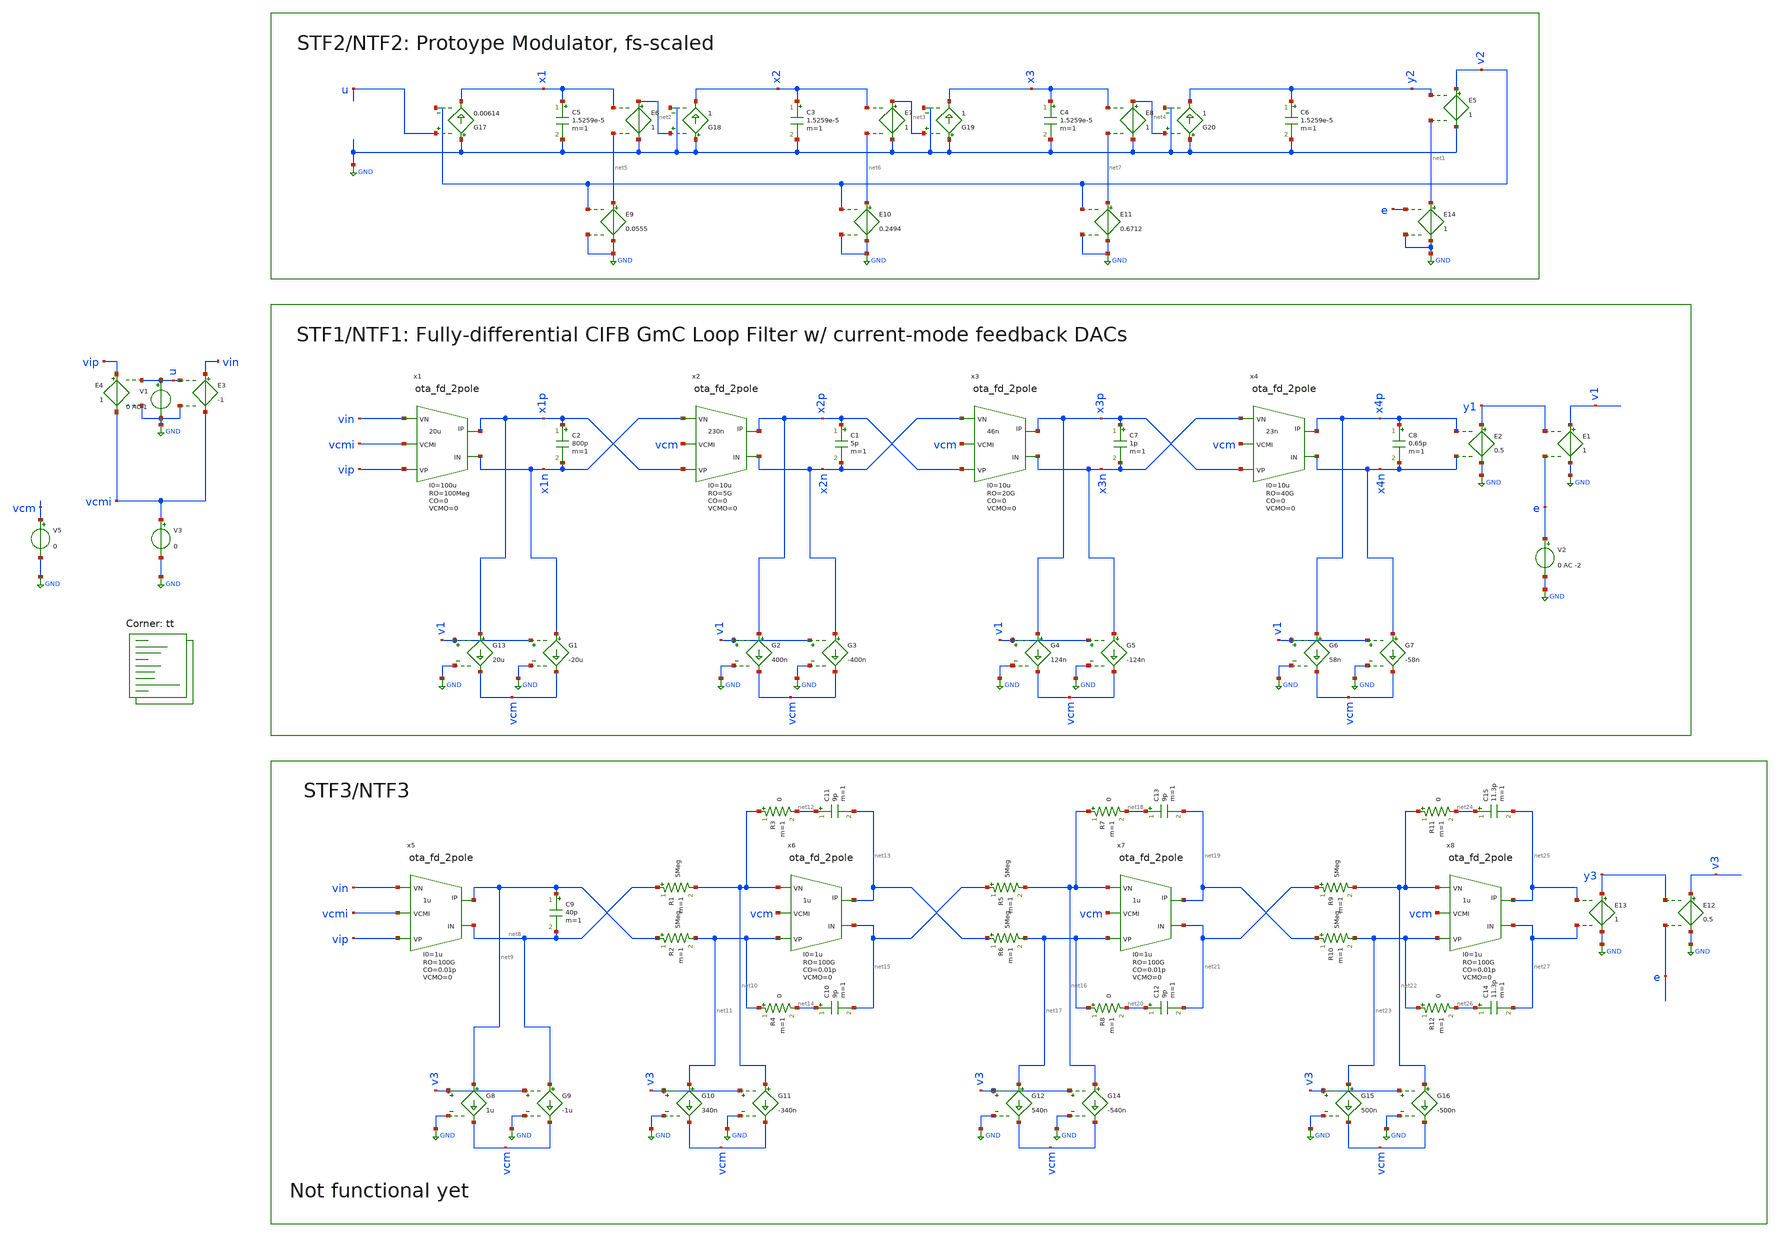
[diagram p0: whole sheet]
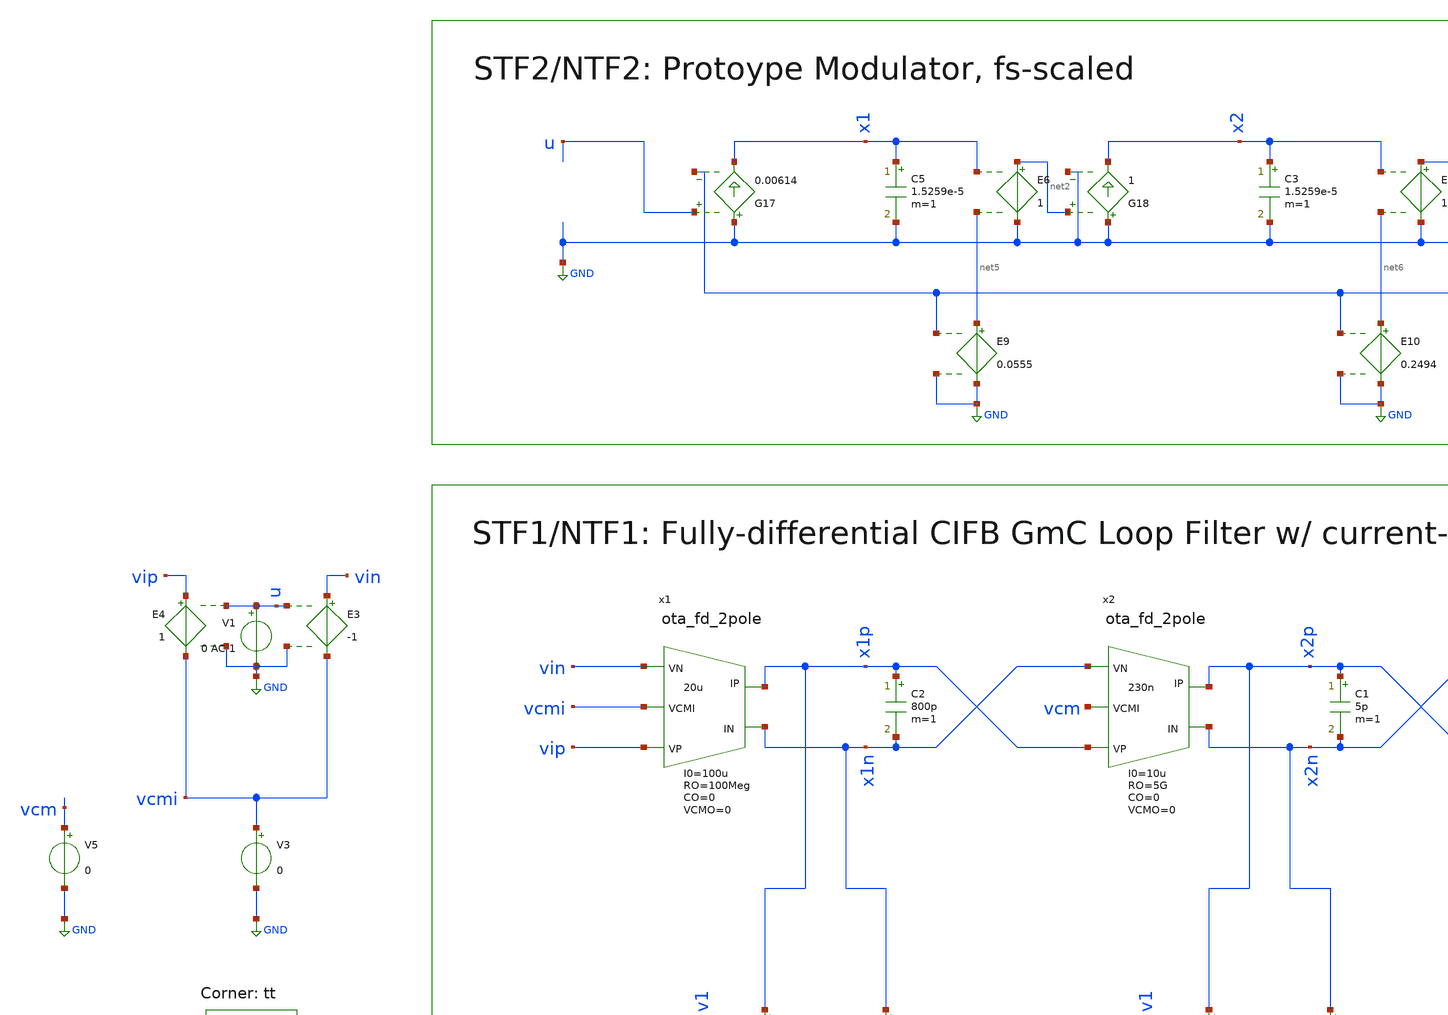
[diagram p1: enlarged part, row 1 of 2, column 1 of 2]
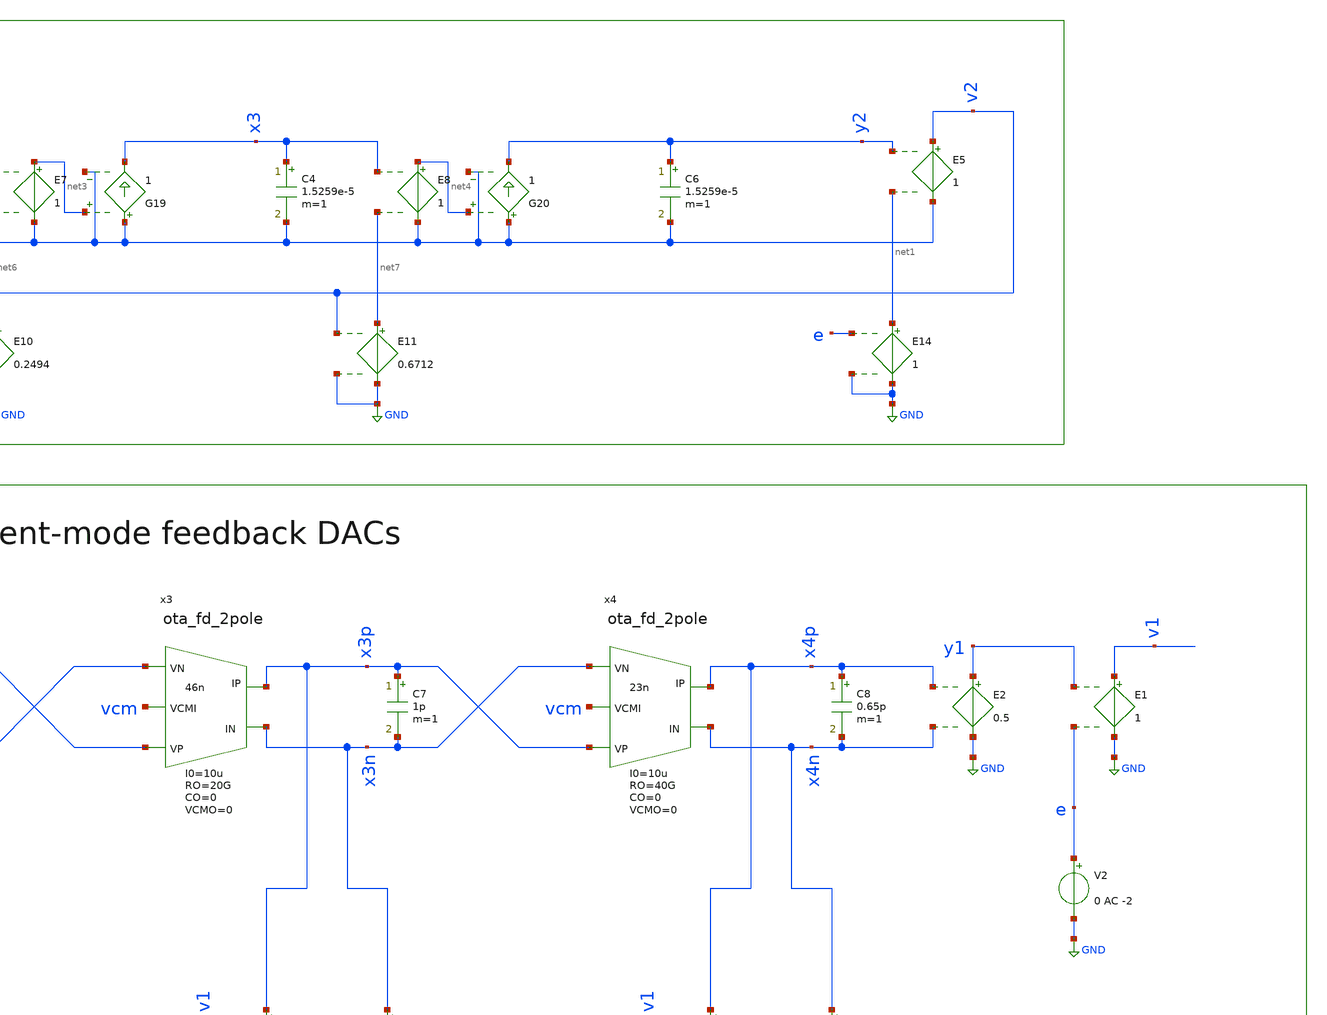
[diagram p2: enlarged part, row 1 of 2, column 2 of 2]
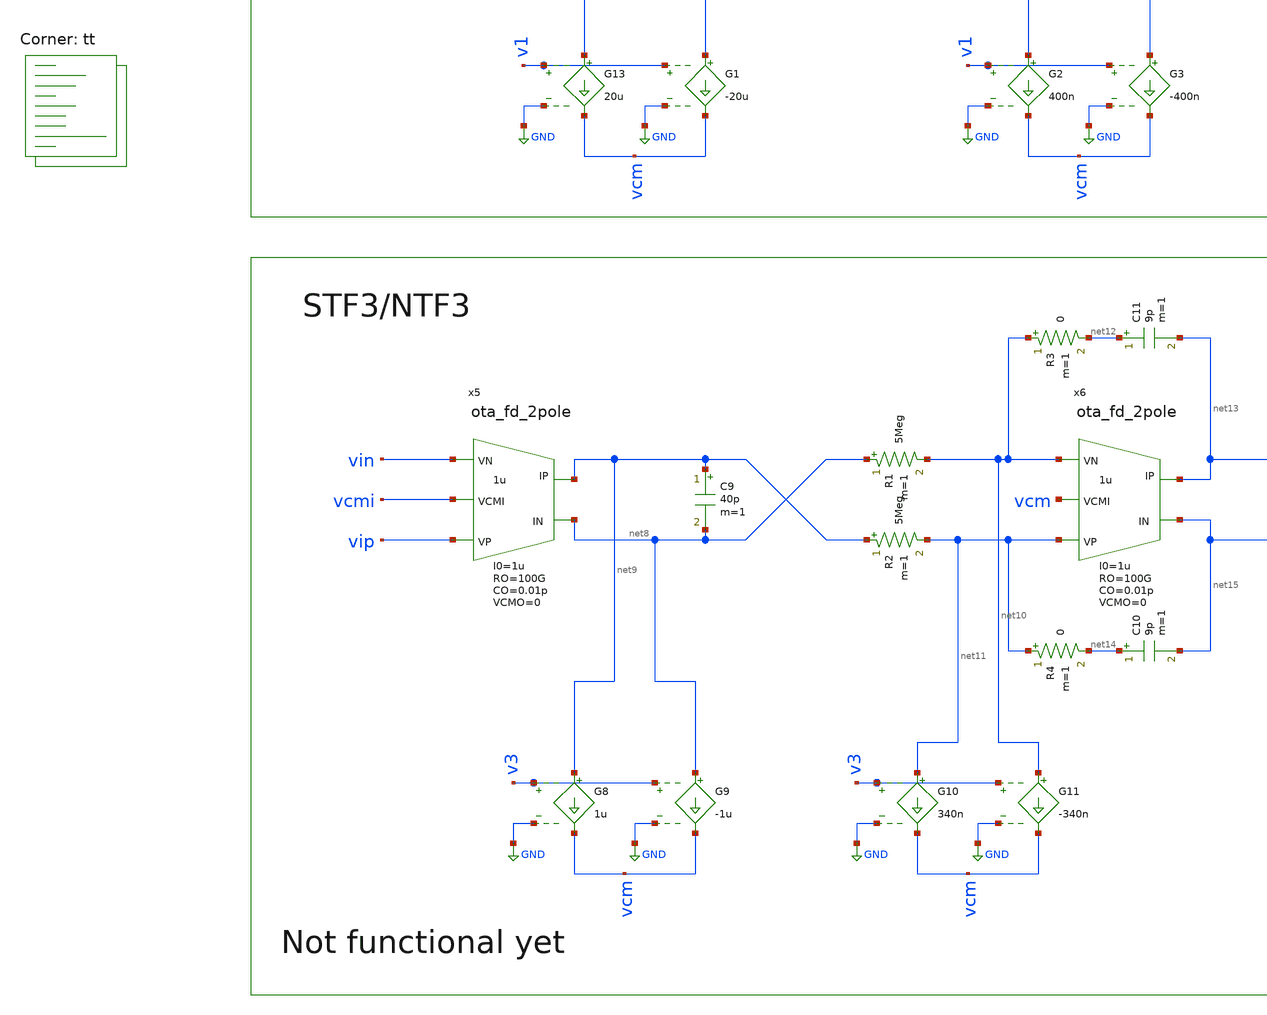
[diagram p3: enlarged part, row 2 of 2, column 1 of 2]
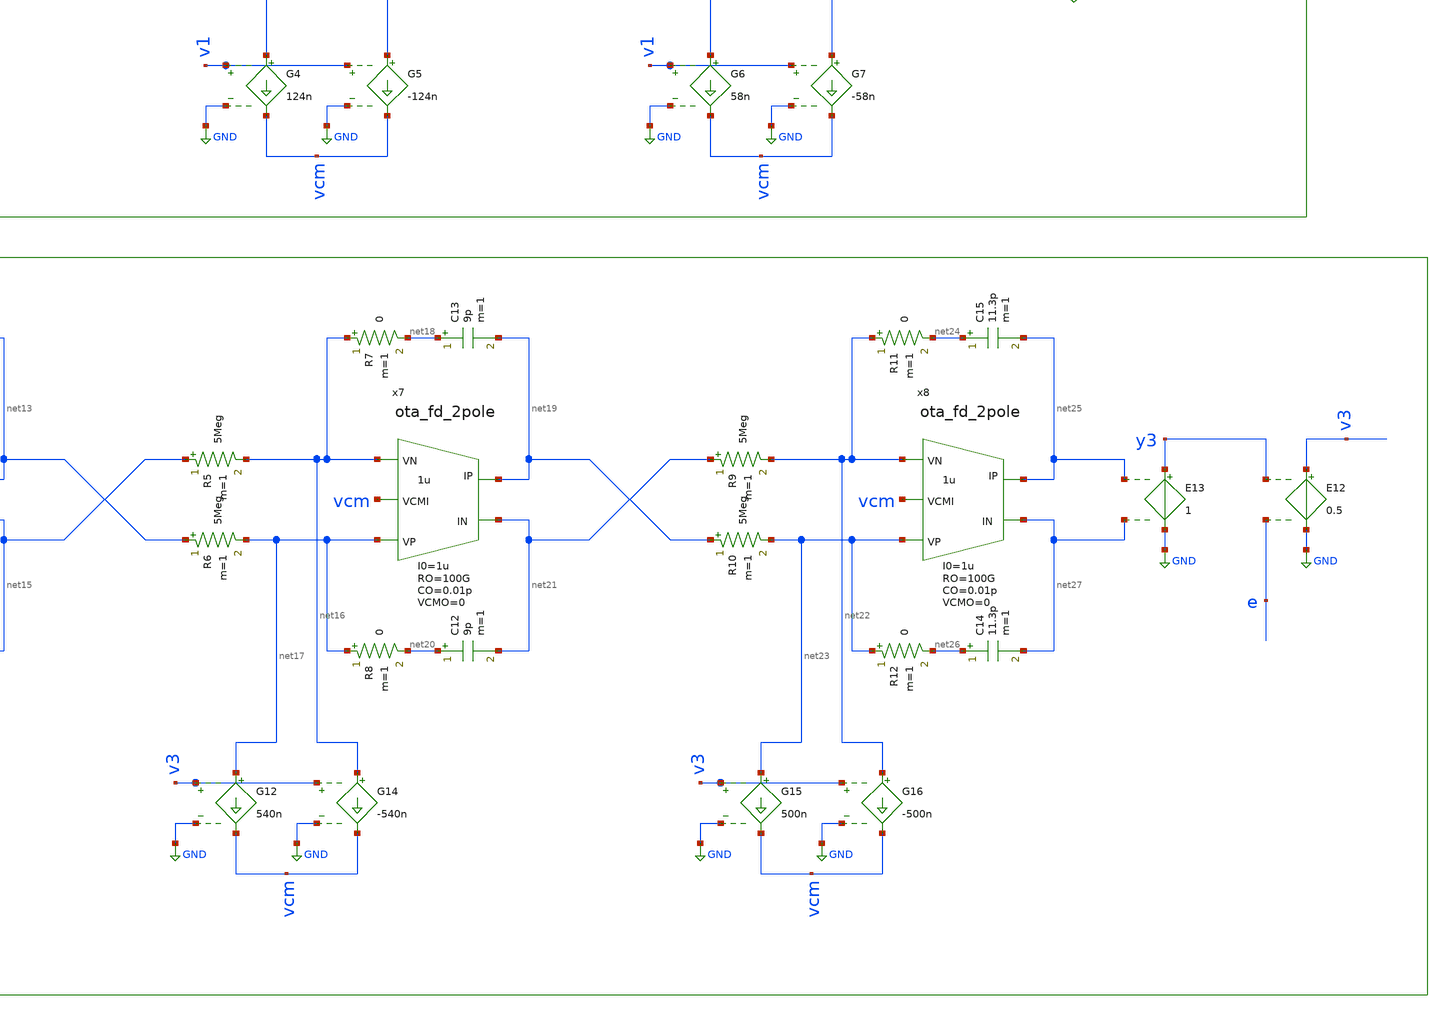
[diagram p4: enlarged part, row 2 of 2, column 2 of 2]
** sch_path: circuit-level/xschem/dsm/dsm_lf_fb_diff_gmc.sch
**.subckt dsm_lf_fb_diff_gmc
V1 u GND 0 AC 1
E1 v1 GND y1 e 1
V2 e GND 0 AC -2
C2 x1p x1n 800p m=1
E2 y1 GND x4p x4n 0.5
V3 vcmi GND 0
E3 vin vcmi u GND -1
E4 vip vcmi u GND 1
V5 vcm GND 0
G13 x1p vcm v1 GND 20u
G1 x1n vcm v1 GND -20u
G17 GND x1 u v2 0.00614
G18 GND x2 net2 GND 1
G19 GND x3 net3 GND 1
C5 x1 GND 1.5259e-5 m=1
C3 x2 GND 1.5259e-5 m=1
C4 x3 GND 1.5259e-5 m=1
E5 v2 GND y2 net1 1
G20 GND y2 net4 GND 1
C6 y2 GND 1.5259e-5 m=1
E6 net2 GND x1 net5 1
E7 net3 GND x2 net6 1
E8 net4 GND x3 net7 1
E9 net5 GND v2 GND 0.0555
E10 net6 GND v2 GND 0.2494
E11 net7 GND v2 GND 0.6712
x1 vin x1p x1n vip vcmi ota_fd_2pole GM=20u RO=100Meg CO=0 RP=0 CP=0 VCMO=0 I0=100u
C1 x2p x2n 5p m=1
G2 x2p vcm v1 GND 400n
G3 x2n vcm v1 GND -400n
x2 x1n x2p x2n x1p vcm ota_fd_2pole GM=230n RO=5G CO=0 RP=0 CP=0 VCMO=0 I0=10u
C7 x3p x3n 1p m=1
G4 x3p vcm v1 GND 124n
G5 x3n vcm v1 GND -124n
x3 x2n x3p x3n x2p vcm ota_fd_2pole GM=46n RO=20G CO=0 RP=0 CP=0 VCMO=0 I0=10u
C8 x4p x4n 0.65p m=1
G6 x4p vcm v1 GND 58n
G7 x4n vcm v1 GND -58n
x4 x3n x4p x4n x3p vcm ota_fd_2pole GM=23n RO=40G CO=0 RP=0 CP=0 VCMO=0 I0=10u
C9 net9 net8 40p m=1
G8 net9 vcm v3 GND 1u
G9 net8 vcm v3 GND -1u
x5 vin net9 net8 vip vcmi ota_fd_2pole GM=1u RO=100G CO=0.01p RP=0 CP=0.1p VCMO=0 I0=1u
R1 net8 net10 5Meg m=1
R2 net9 net11 5Meg m=1
x6 net10 net13 net15 net11 vcm ota_fd_2pole GM=1u RO=100G CO=0.01p RP=0 CP=0.1p VCMO=0 I0=1u
R3 net10 net12 0 m=1
R4 net11 net14 0 m=1
C10 net14 net15 9p m=1
C11 net12 net13 9p m=1
G10 net11 vcm v3 GND 340n
G11 net10 vcm v3 GND -340n
R5 net15 net16 5Meg m=1
R6 net13 net17 5Meg m=1
x7 net16 net19 net21 net17 vcm ota_fd_2pole GM=1u RO=100G CO=0.01p RP=0 CP=0.1p VCMO=0 I0=1u
R7 net16 net18 0 m=1
R8 net17 net20 0 m=1
C12 net20 net21 9p m=1
C13 net18 net19 9p m=1
G12 net17 vcm v3 GND 540n
G14 net16 vcm v3 GND -540n
R9 net21 net22 5Meg m=1
R10 net19 net23 5Meg m=1
x8 net22 net25 net27 net23 vcm ota_fd_2pole GM=1u RO=100G CO=0.01p RP=0 CP=0.1p VCMO=0 I0=1u
R11 net22 net24 0 m=1
R12 net23 net26 0 m=1
C14 net26 net27 11.3p m=1
C15 net24 net25 11.3p m=1
G15 net23 vcm v3 GND 500n
G16 net22 vcm v3 GND -500n
E12 v3 GND y3 e 0.5
E13 y3 GND net25 net27 1
E14 net1 GND e GND 1
**** begin user architecture code
.lib $::SKYWATER_MODELS/sky130.lib.spice tt


.options savecurrents
.control
save all

** Main Simulations
let pltnr = 1
let runnr = 1
let stop = 1

let fs = 65536
let fmax = fs/2
let fmin = fs*1e-4

set wr_singlescale
set wr_vecnames
option numdgt=5

while const.runnr le const.stop

	alter @V1[ac] = 1
	alter @V2[ac] = 0
	ac dec 100 $&fmin $&fmax
	alter @V1[ac] = 0
	alter @V2[ac] = -1
	ac dec 100 $&fmin $&fmax

	set pltName = ac$&const.pltnr
       	setplot $pltName

	let stf_1 = v1/u
	let stf_2 = v2/u
	let stf_3 = v3/u
	plot vdb(stf_1) vdb(stf_2) vdb(stf_3)

	let pltnr = const.pltnr + 1
	set pltName = ac$&const.pltnr
       	setplot $pltName

	let ntf_gmc_fd = (v1/e)+1e-15
	let ntf_ref_se = (v2/e)+1e-15
	let ntf_rcota_fd = (v3/e)+1e-15
	plot vdb(ntf_gmc_fd) vdb(ntf_ref_se)
	*vdb(ntf_rcota_fd)

	let ntf_gmc_fd_db = vdb(ntf_gmc_fd)
	let ntf_ref_se_db = vdb(ntf_ref_se)

	wrdata /foss/designs/ntf_verify_fd.txt ntf_gmc_fd_db ntf_ref_se_db

       	let pltnr = const.pltnr + 1
	let runnr = const.runnr + 1
end

remzerovec
op
write dsm_lf_fb_diff_gmc.raw
.endc

**** end user architecture code
**.ends

* expanding   symbol:  /foss/designs/macro-models/ota_fd_2pole.sym # of pins=5
** sym_path: circuit-level/xschem/macro-models/ota_fd_2pole.sym
** sch_path: circuit-level/xschem/macro-models/ota_fd_2pole.sch
.subckt ota_fd_2pole VN IP IN VP VCMI  GM=1u RO=100Meg CO=1p RP=0 CP=0.1p VCMO=0 I0=1u
*.ipin VP
*.ipin VN
*.opin IP
*.opin IN
*.ipin VCMI
R3 IP net1 {{RO}/2} m=1
R4 IN net1 {{RO}/2} m=1
C3 IP net1 {2*{CO}} m=1
R5 VN ip1 {RP} m=1
C4 ip1 VCMI {CP} m=1
C6 in1 VCMI {CP} m=1
C8 IN net1 {2*{CO}} m=1
R7 VP in1 {RP} m=1
B2 IP net1 I = {{I0}*tanh({GM}/2*V(ip1,in1)/{I0})}
B1 net1 IN I = {{I0}*tanh({GM}/2*V(ip1,in1)/{I0})}
B5 net1 GND I = {{VCMO}-(V(IP)+V(IN))/2}
.ends

.GLOBAL GND
.end
